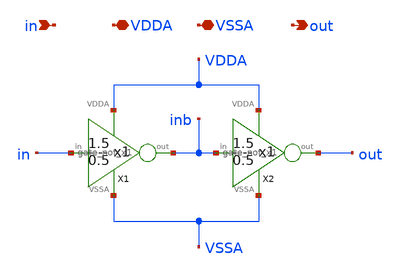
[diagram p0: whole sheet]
** sch_path: sky130A/analog/gate_buffer_x1.sch
**.subckt gate_buffer_x1 in out VDDA VSSA
*.ipin in
*.opin out
*.iopin VDDA
*.iopin VSSA
X1 in inb VDDA VSSA gate_not_x1
X2 inb out VDDA VSSA gate_not_x1
**.ends

* expanding   symbol:  gate_not_x1.sym # of pins=4
** sym_path: sky130A/analog/gate_not_x1.sym
** sch_path: sky130A/analog/gate_not_x1.sch
.subckt gate_not_x1 in out VDDA VSSA
*.ipin in
*.iopin VDDA
*.iopin VSSA
*.opin out
XM1 out in VSSA VSSA sky130_fd_pr__nfet_01v8 L=0.15 W=0.5 nf=1 ad='int((1 + 1)/2) * 0.5 / 1 * 0.29' as='int((1 + 2)/2) * 0.5 / 1 * 0.29'
+ pd='2*int((1 + 1)/2) * (0.5 / 1 + 0.29)' ps='2*int((1 + 2)/2) * (0.5 / 1 + 0.29)' nrd='0.29 / 0.5 ' nrs='0.29 / 0.5 '
+ sa=0 sb=0 sd=0 mult=1 m=1
XM2 out in VDDA VDDA sky130_fd_pr__pfet_01v8 L=0.15 W=1.5 nf=1 ad='int((1 + 1)/2) * 1.5 / 1 * 0.29' as='int((1 + 2)/2) * 1.5 / 1 * 0.29'
+ pd='2*int((1 + 1)/2) * (1.5 / 1 + 0.29)' ps='2*int((1 + 2)/2) * (1.5 / 1 + 0.29)' nrd='0.29 / 1.5 ' nrs='0.29 / 1.5 '
+ sa=0 sb=0 sd=0 mult=1 m=1
.ends

.end
